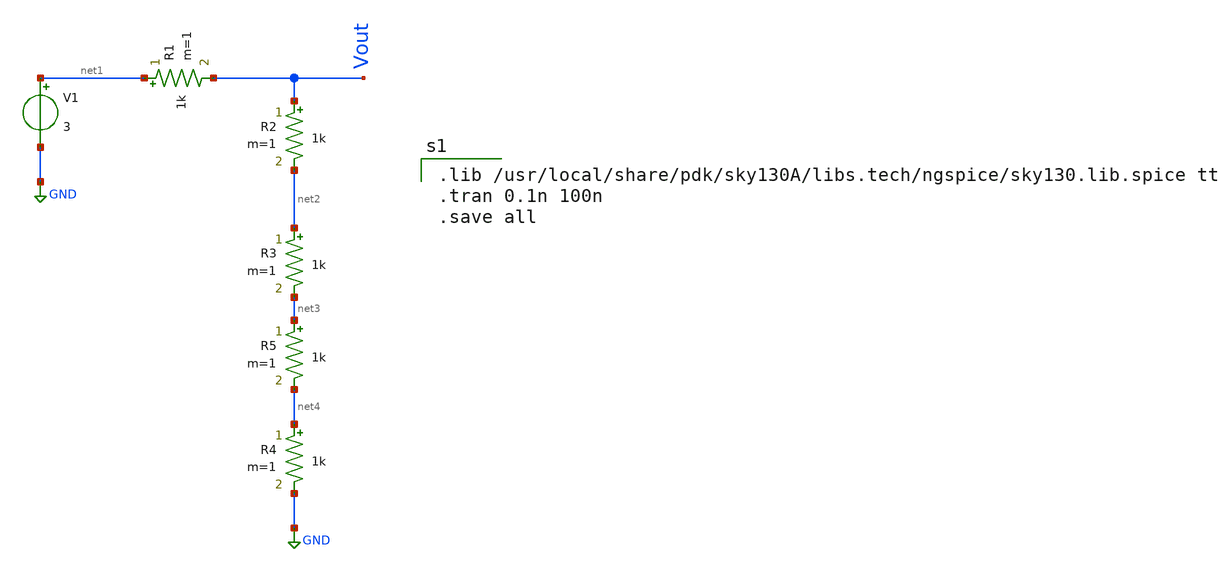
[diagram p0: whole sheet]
** sch_path: Schematic/VoltageDivider.sch
**.subckt VoltageDivider
R1 net1 Vout 1k m=1
V1 net1 GND 3
R3 net2 net3 1k m=1
R2 Vout net2 1k m=1
R4 net4 GND 1k m=1
R5 net3 net4 1k m=1
**** begin user architecture code

.lib /usr/local/share/pdk/sky130A/libs.tech/ngspice/sky130.lib.spice tt
.tran 0.1n 100n
.save all




**** end user architecture code
**.ends
.GLOBAL GND
.end
